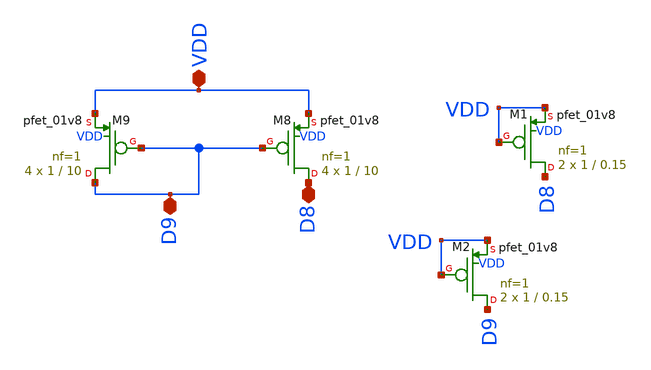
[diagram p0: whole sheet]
** sch_path: magic/pmos_current_tt.sch
**.subckt pmos_current_tt VDD D9 D8
*.iopin VDD
*.iopin D9
*.iopin D8
XM8 D8 D9 VDD VDD sky130_fd_pr__pfet_01v8 L=10 W=1 nf=1 ad='int((nf+1)/2) * W/nf * 0.29' as='int((nf+2)/2) * W/nf * 0.29'
+ pd='2*int((nf+1)/2) * (W/nf + 0.29)' ps='2*int((nf+2)/2) * (W/nf + 0.29)' nrd='0.29 / W' nrs='0.29 / W'
+ sa=0 sb=0 sd=0 mult=4 m=4
XM9 D9 D9 VDD VDD sky130_fd_pr__pfet_01v8 L=10 W=1 nf=1 ad='int((nf+1)/2) * W/nf * 0.29' as='int((nf+2)/2) * W/nf * 0.29'
+ pd='2*int((nf+1)/2) * (W/nf + 0.29)' ps='2*int((nf+2)/2) * (W/nf + 0.29)' nrd='0.29 / W' nrs='0.29 / W'
+ sa=0 sb=0 sd=0 mult=4 m=4
XM1 D8 VDD VDD VDD sky130_fd_pr__pfet_01v8 L=0.15 W=1 nf=1 ad='int((nf+1)/2) * W/nf * 0.29' as='int((nf+2)/2) * W/nf * 0.29'
+ pd='2*int((nf+1)/2) * (W/nf + 0.29)' ps='2*int((nf+2)/2) * (W/nf + 0.29)' nrd='0.29 / W' nrs='0.29 / W'
+ sa=0 sb=0 sd=0 mult=2 m=2
XM2 D9 VDD VDD VDD sky130_fd_pr__pfet_01v8 L=0.15 W=1 nf=1 ad='int((nf+1)/2) * W/nf * 0.29' as='int((nf+2)/2) * W/nf * 0.29'
+ pd='2*int((nf+1)/2) * (W/nf + 0.29)' ps='2*int((nf+2)/2) * (W/nf + 0.29)' nrd='0.29 / W' nrs='0.29 / W'
+ sa=0 sb=0 sd=0 mult=2 m=2
**.ends
.end
